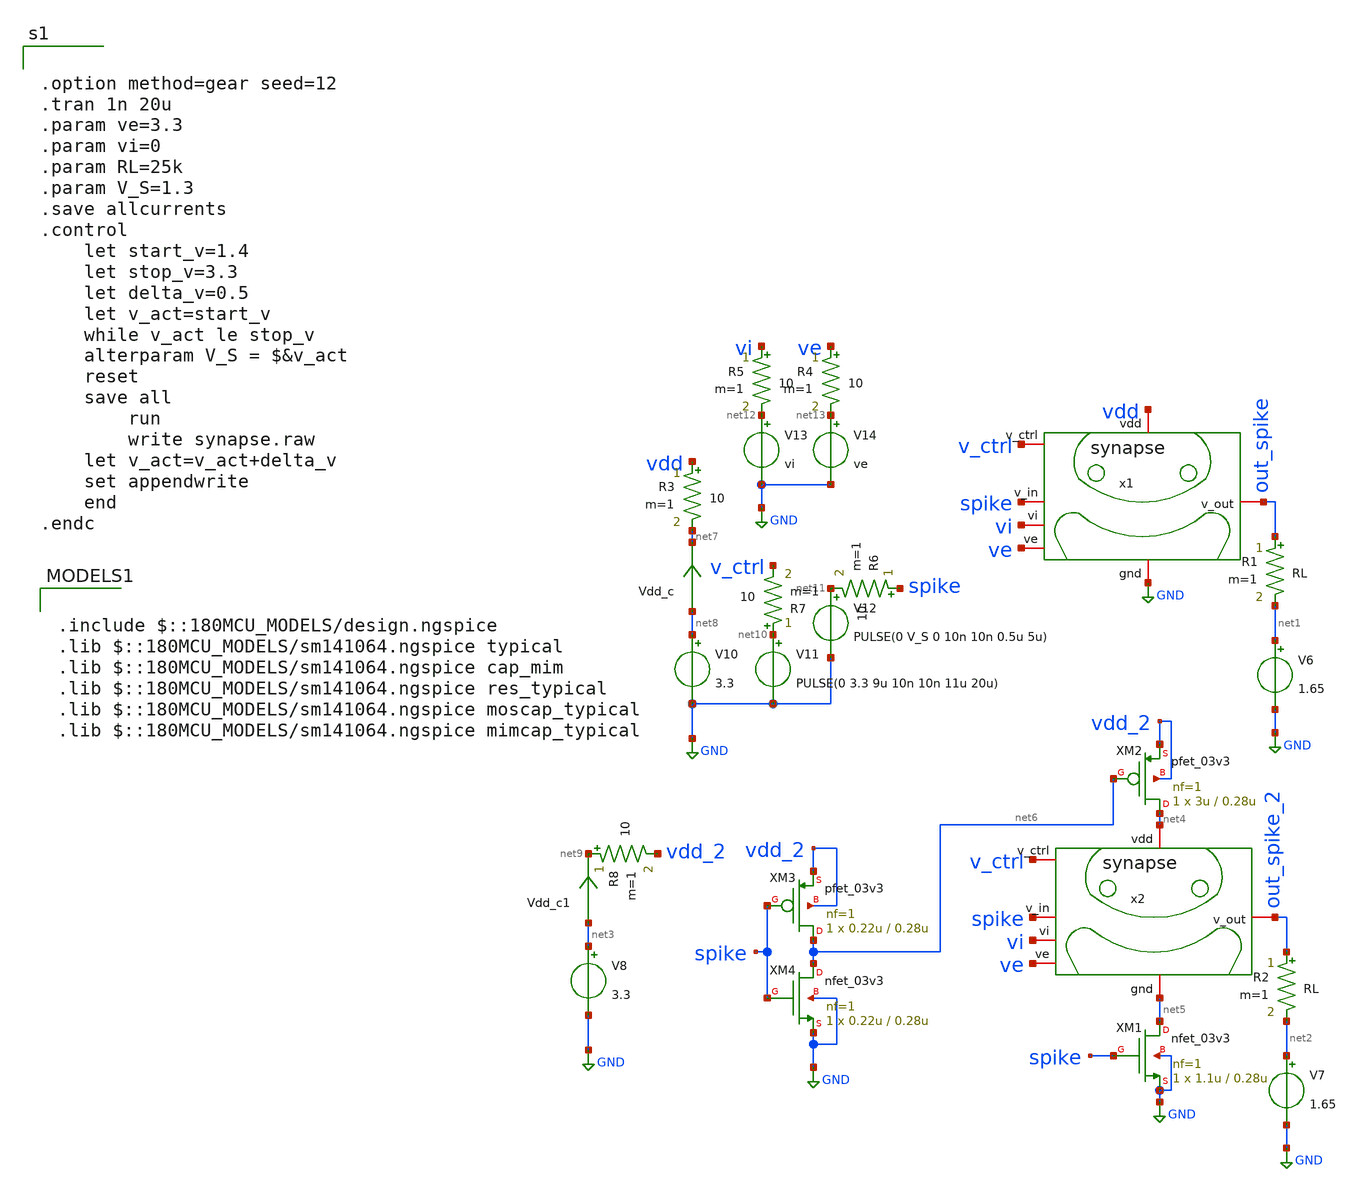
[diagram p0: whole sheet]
** sch_path: designs/libs/tb_core_analogs/tb_synapse_pc/synapse_pc.sch
**.subckt synapse_pc
V6 net1 GND 1.65
R1 out_spike net1 RL m=1
x1 vdd spike ve v_ctrl out_spike vi GND synapse
V7 net2 GND 1.65
R2 out_spike_2 net2 RL m=1
x2 net4 spike ve v_ctrl out_spike_2 vi net5 synapse
V8 net3 GND 3.3
Vdd_c1 net3 net9 0
.save i(vdd_c1)
XM1 net5 spike GND GND nfet_03v3 L=0.28u W=1.1u nf=1 ad='int((nf+1)/2) * W/nf * 0.18u' as='int((nf+2)/2) * W/nf * 0.18u'
+ pd='2*int((nf+1)/2) * (W/nf + 0.18u)' ps='2*int((nf+2)/2) * (W/nf + 0.18u)' nrd='0.18u / W' nrs='0.18u / W'
+ sa=0 sb=0 sd=0 m=1
XM2 net4 net6 vdd_2 vdd_2 pfet_03v3 L=0.28u W=3u nf=1 ad='int((nf+1)/2) * W/nf * 0.18u' as='int((nf+2)/2) * W/nf * 0.18u'
+ pd='2*int((nf+1)/2) * (W/nf + 0.18u)' ps='2*int((nf+2)/2) * (W/nf + 0.18u)' nrd='0.18u / W' nrs='0.18u / W'
+ sa=0 sb=0 sd=0 m=1
XM3 net6 spike vdd_2 vdd_2 pfet_03v3 L=0.28u W=0.22u nf=1 ad='int((nf+1)/2) * W/nf * 0.18u' as='int((nf+2)/2) * W/nf * 0.18u'
+ pd='2*int((nf+1)/2) * (W/nf + 0.18u)' ps='2*int((nf+2)/2) * (W/nf + 0.18u)' nrd='0.18u / W' nrs='0.18u / W'
+ sa=0 sb=0 sd=0 m=1
XM4 net6 spike GND GND nfet_03v3 L=0.28u W=0.22u nf=1 ad='int((nf+1)/2) * W/nf * 0.18u' as='int((nf+2)/2) * W/nf * 0.18u'
+ pd='2*int((nf+1)/2) * (W/nf + 0.18u)' ps='2*int((nf+2)/2) * (W/nf + 0.18u)' nrd='0.18u / W' nrs='0.18u / W'
+ sa=0 sb=0 sd=0 m=1
V10 net8 GND 3.3
Vdd_c net8 net7 0
.save i(vdd_c)
V11 net10 GND PULSE(0 3.3 9u 10n 10n 11u 20u)
V12 net11 GND PULSE(0 V_S 0 10n 10n 0.5u 5u)
V13 net12 GND vi
V14 net13 GND ve
R3 vdd net7 10 m=1
R4 ve net13 10 m=1
R5 vi net12 10 m=1
R6 spike net11 10 m=1
R7 net10 v_ctrl 10 m=1
R8 net9 vdd_2 10 m=1
**** begin user architecture code


.option method=gear seed=12
.tran 1n 20u
.param ve=3.3
.param vi=0
.param RL=25k
.param V_S=1.3
.save allcurrents
.control
    let start_v=1.4
    let stop_v=3.3
    let delta_v=0.5
    let v_act=start_v
    while v_act le stop_v
	alterparam V_S = $&v_act
	reset
	save all
        run
        write synapse.raw
	let v_act=v_act+delta_v
	set appendwrite
    end
.endc



.include $::180MCU_MODELS/design.ngspice
.lib $::180MCU_MODELS/sm141064.ngspice typical
.lib $::180MCU_MODELS/sm141064.ngspice cap_mim
.lib $::180MCU_MODELS/sm141064.ngspice res_typical
.lib $::180MCU_MODELS/sm141064.ngspice moscap_typical
.lib $::180MCU_MODELS/sm141064.ngspice mimcap_typical

**** end user architecture code
**.ends
.GLOBAL GND
.end
